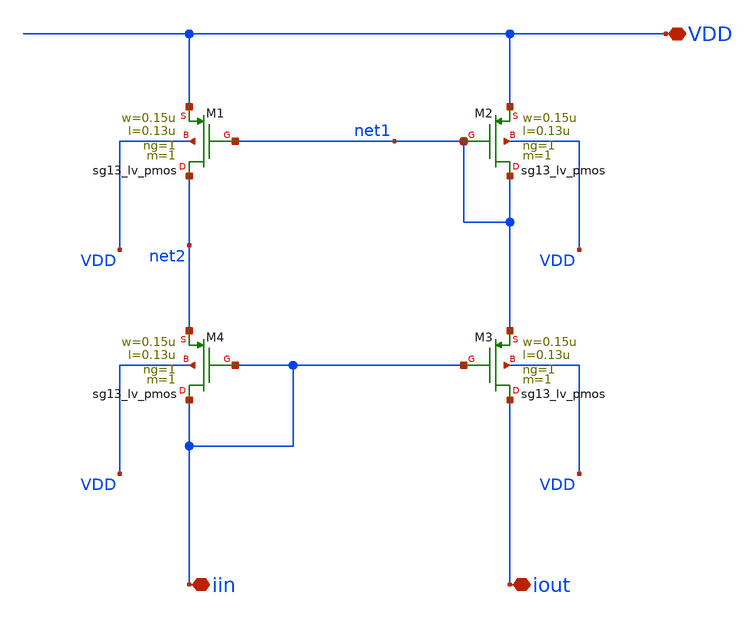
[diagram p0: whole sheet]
** sch_path: analog-db/templates/current_mirror/pmos_current_source/improved_wilson_current_mirror.sch
**.subckt improved_wilson_current_mirror VDD iout iin
*.iopin VDD
*.iopin iout
*.iopin iin
XM1 net2 net1 VDD VDD sg13_lv_pmos w=0.15u l=0.13u ng=1 m=1 mm_ok=1
XM2 net1 net1 VDD VDD sg13_lv_pmos w=0.15u l=0.13u ng=1 m=1 mm_ok=1
XM3 iout iin net1 VDD sg13_lv_pmos w=0.15u l=0.13u ng=1 m=1 mm_ok=1
XM4 iin iin net2 VDD sg13_lv_pmos w=0.15u l=0.13u ng=1 m=1 mm_ok=1
**.ends
.end
